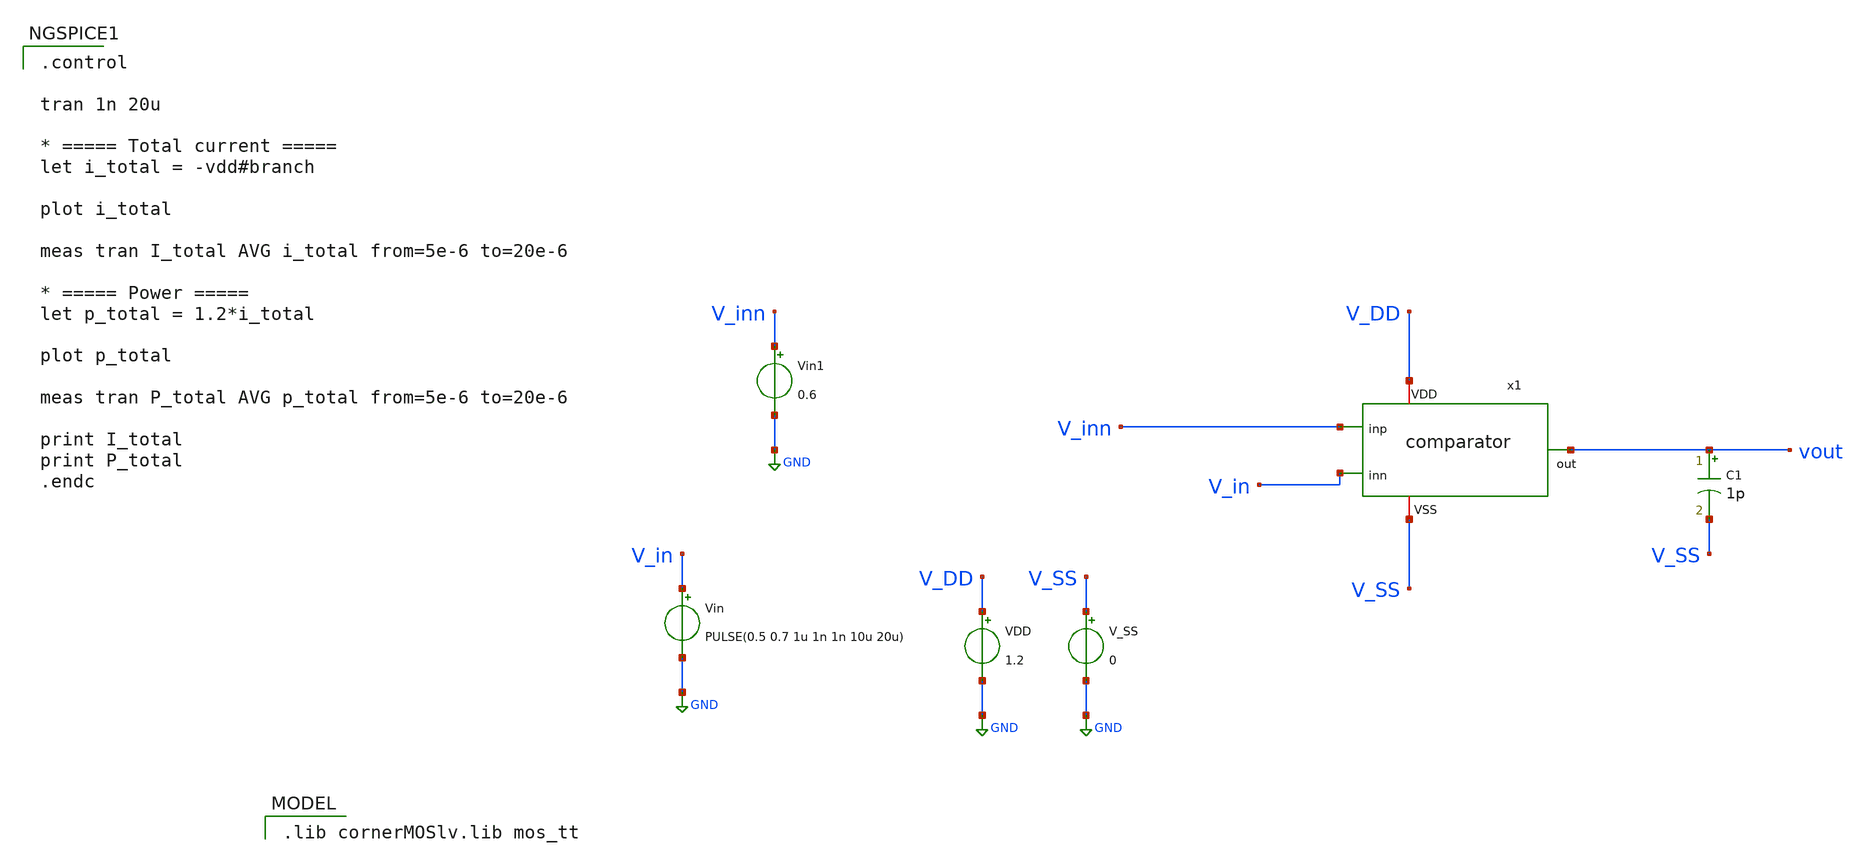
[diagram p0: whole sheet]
** sch_path: xschem/comparator_tb_power_consumption.sch
**.subckt comparator_tb_power_consumption
C1 vout V_SS 1p m=1
Vin V_in GND PULSE(0.5 0.7 1u 1n 1n 10u 20u)
VDD V_DD GND 1.2
V_SS V_SS GND 0
x1 V_DD vout V_in V_inn V_SS comparator
Vin1 V_inn GND 0.6
**** begin user architecture code
 .lib cornerMOSlv.lib mos_tt


.control

tran 1n 20u

* ===== Total current =====
let i_total = -vdd#branch

plot i_total

meas tran I_total AVG i_total from=5e-6 to=20e-6

* ===== Power =====
let p_total = 1.2*i_total

plot p_total

meas tran P_total AVG p_total from=5e-6 to=20e-6

print I_total
print P_total
.endc


**** end user architecture code
**.ends

* expanding   symbol:  comparator.sym # of pins=5
** sym_path: xschem/comparator.sym
** sch_path: xschem/comparator.sch
.subckt comparator VDD out inn inp VSS
*.ipin inp
*.ipin inn
*.iopin VDD
*.iopin VSS
*.opin out
XM4 net2 net1 VDD VDD sg13_lv_pmos w=1.5u l=5u ng=1 m=1 mm_ok=1
XM3 net1 net1 VDD VDD sg13_lv_pmos w=1.5u l=5u ng=1 m=1 mm_ok=1
XM1 net1 inp net3 VSS sg13_lv_nmos w=1.5u l=5u ng=1 m=1 mm_ok=1
XM2 net2 inn net3 VSS sg13_lv_nmos w=1.5u l=5u ng=1 m=1 mm_ok=1
XM7 net4 net4 VDD VDD sg13_lv_pmos w=1.5u l=5u ng=1 m=1 mm_ok=1
XM8 out net2 VDD VDD sg13_lv_pmos w=1.5u l=5u ng=1 m=1 mm_ok=1
XM6 net4 net4 VSS VSS sg13_lv_nmos w=2.5u l=5u ng=1 m=1 mm_ok=1
XM5 net3 net4 VSS VSS sg13_lv_nmos w=1.5u l=5u ng=1 m=1 mm_ok=1
XM9 out net4 VSS VSS sg13_lv_nmos w=1.5u l=5u ng=1 m=1 mm_ok=1
.ends

.GLOBAL GND
.end
